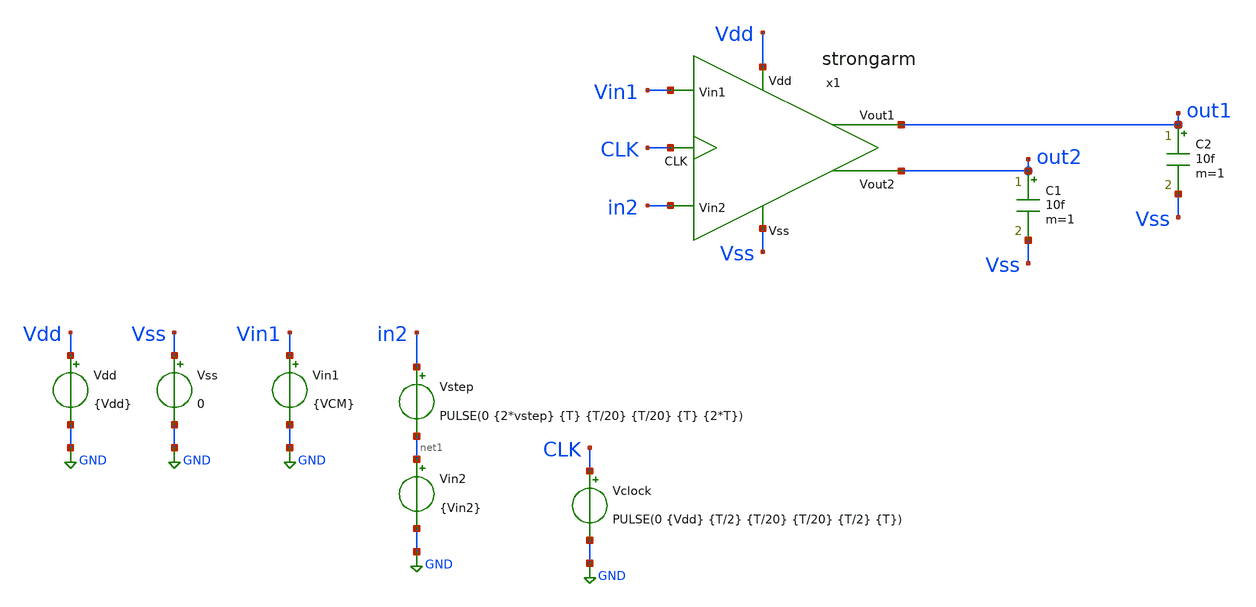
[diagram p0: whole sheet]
** sch_path: xschem/TB/TB_Tran_SA.sch
**.subckt TB_Tran_SA
Vdd Vdd GND {Vdd}
x1 out2 out1 Vdd Vss in2 Vin1 CLK strongarm
Vss Vss GND 0
C1 out2 Vss 10f m=1
C2 out1 Vss 10f m=1
Vin1 Vin1 GND {VCM}
Vin2 net1 GND {Vin2}
Vclock CLK GND PULSE(0 {Vdd} {T/2} {T/20} {T/20} {T/2} {T})
Vstep in2 net1 PULSE(0 {2*vstep} {T} {T/20} {T/20} {T} {2*T})
**** begin user architecture code


.param Vdd   = 1.8
.param VCM   = 0.9
.param Vstep = 1m
.param Vin2  = VCM-Vstep
.ic V(out1) = 1.8
.ic V(out2) = 1.8
.ic V(x1.common) = 1.8
.ic V(x1.P) = 1.8
.ic V(x1.Q) = 1.8





.lib cornerMOSlv.lib mos_tt




.param T = 300p
.control
save all  @n.x1.xm3.nsg13_lv_nmos[vgs]  @n.x1.xm4.nsg13_lv_nmos[vgs]  @n.x1.xm5.nsg13_lv_pmos[vgs]
+  @n.x1.xm6.nsg13_lv_pmos[vgs]  @n.x1.xm10.nsg13_lv_pmos[vgs]  @n.x1.xm11.nsg13_lv_pmos[vgs]
*  @n.x1.xm10.nsg13_lv_pmos[vgt]  @n.x1.xm10.nsg13_lv_pmos[vth]  @n.x1.xm7.nsg13_lv_nmos[vds]
*  @n.x1.xm1.nsg13_lv_nmos[ids]  @n.x1.xm2.nsg13_lv_nmos[ids]  @n.x1.xm3.nsg13_lv_nmos[ids]
*+  @n.x1.xm7.nsg13_lv_nmos[ids]  @n.x1.xm10.nsg13_lv_pmos[ids]  @n.x1.xm11.nsg13_lv_pmos[ids]
*  @n.x1.xm1.nsg13_lv_nmos[gds]  @n.x1.xm2.nsg13_lv_nmos[gds]  @n.x1.xm7.nsg13_lv_nmos[gds]

tran 0.1p 900p
let vgs3 = @n.x1.xm3.nsg13_lv_nmos[vgs]
let vgs4 = @n.x1.xm4.nsg13_lv_nmos[vgs]
let vgs5 = @n.x1.xm5.nsg13_lv_pmos[vgs]
let vgs6 = @n.x1.xm6.nsg13_lv_pmos[vgs]
let vgsa = @n.x1.xm10.nsg13_lv_pmos[vgs]
let vgsb = @n.x1.xm11.nsg13_lv_pmos[vgs]

let vgta = @n.x1.xm10.nsg13_lv_pmos[vgt]
let vtha = @n.x1.xm10.nsg13_lv_pmos[vth]

let id1 = @n.x1.xm1.nsg13_lv_nmos[ids]
let id2 = @n.x1.xm2.nsg13_lv_nmos[ids]
let id7 = @n.x1.xm7.nsg13_lv_nmos[ids]
let id10 = @n.x1.xm10.nsg13_lv_pmos[ids]
let id11 = @n.x1.xm11.nsg13_lv_pmos[ids]

let rds1 = 1/@n.x1.xm1.nsg13_lv_nmos[gds]
let rds2 = 1/@n.x1.xm2.nsg13_lv_nmos[gds]
let rds7 = 1/@n.x1.xm7.nsg13_lv_nmos[gds]
let Pot = id7*@n.x1.xm7.nsg13_lv_nmos[vds]

meas tran Amp_t TRIG v(out1) VAL=1.79 CROSS=1 TARG v(out1) VAL=0.9 CROSS=1
meas tran reg_t TRIG v(out1) VAL=0.9  CROSS=1 TARG v(out1) VAL=0.01 CROSS=1
meas tran Energy INTEG Pot from=140p to=300p
meas tran Avg_Power AVG Pot from=140p to=300p
*plot v(x1.Q) v(x1.P) v(clk)
*plot v(x1.common) v(clk)
plot v(out1) v(out2) v(clk)+2 (v(in2)-899m)*500+2
plot v(x1.Q) v(x1.P)
.endc




** TRANSISTORES NMOS

.param W12 = 0.25u
.param L12 = 0.75u
.param M12 = 120

.param W34 = 0.25u
.param L34 = 0.13u
.param M34 = 50

.param W56 = 0.25u
.param L56 = 0.13u
.param M56 = 10

.param W7  = 0.25u
.param L7  = 0.13u
.param M7  = 110

.param W89 = 0.25u
.param L89 = 0.13u
.param M89 = 17

.param Wab = 0.25u
.param Lab = 0.13u
.param Mab = 20


**** end user architecture code
**.ends

* expanding   symbol:  ../sch/strongarm.sym # of pins=7
** sym_path: xschem/sch/strongarm.sym
** sch_path: xschem/sch/strongarm.sch
.subckt strongarm Vout2 Vout1 Vdd Vss Vin2 Vin1 CLK
*.opin Vout2
*.opin Vout1
*.ipin Vin1
*.ipin Vin2
*.ipin CLK
*.ipin Vss
*.ipin Vdd
XM1 common Vin1 P Vss sg13_lv_nmos w={W12} l={L12} ng=1 m={M12} mm_ok=1
XM2 common Vin2 Q Vss sg13_lv_nmos w={W12} l={L12} ng=1 m={M12} mm_ok=1
XM3 P Vout2 Vout1 Vss sg13_lv_nmos w={W34} l={L34} ng=1 m={M34} mm_ok=1
XM4 Q Vout1 Vout2 Vss sg13_lv_nmos w={W34} l={L34} ng=1 m={M34} mm_ok=1
XM6 Vout2 Vout1 Vdd Vdd sg13_lv_pmos w={W56} l={L56} ng=1 m={M56} mm_ok=1
XM5 Vout1 Vout2 Vdd Vdd sg13_lv_pmos w={W56} l={L56} ng=1 m={M56} mm_ok=1
XM7 Vss CLK common Vss sg13_lv_nmos w={W7} l={L7} ng=1 m={M7} mm_ok=1
XM8 P CLK Vdd Vdd sg13_lv_pmos w={W89} l={L89} ng=1 m={M89} mm_ok=1
XM9 Q CLK Vdd Vdd sg13_lv_pmos w={W89} l={L89} ng=1 m={M89} mm_ok=1
XM11 Vdd CLK Vout2 Vdd sg13_lv_pmos w={Wab} l={Lab} ng=1 m={Mab} mm_ok=1
XM10 Vdd CLK Vout1 Vdd sg13_lv_pmos w={Wab} l={Lab} ng=1 m={Mab} mm_ok=1
.ends

.GLOBAL GND
.end
